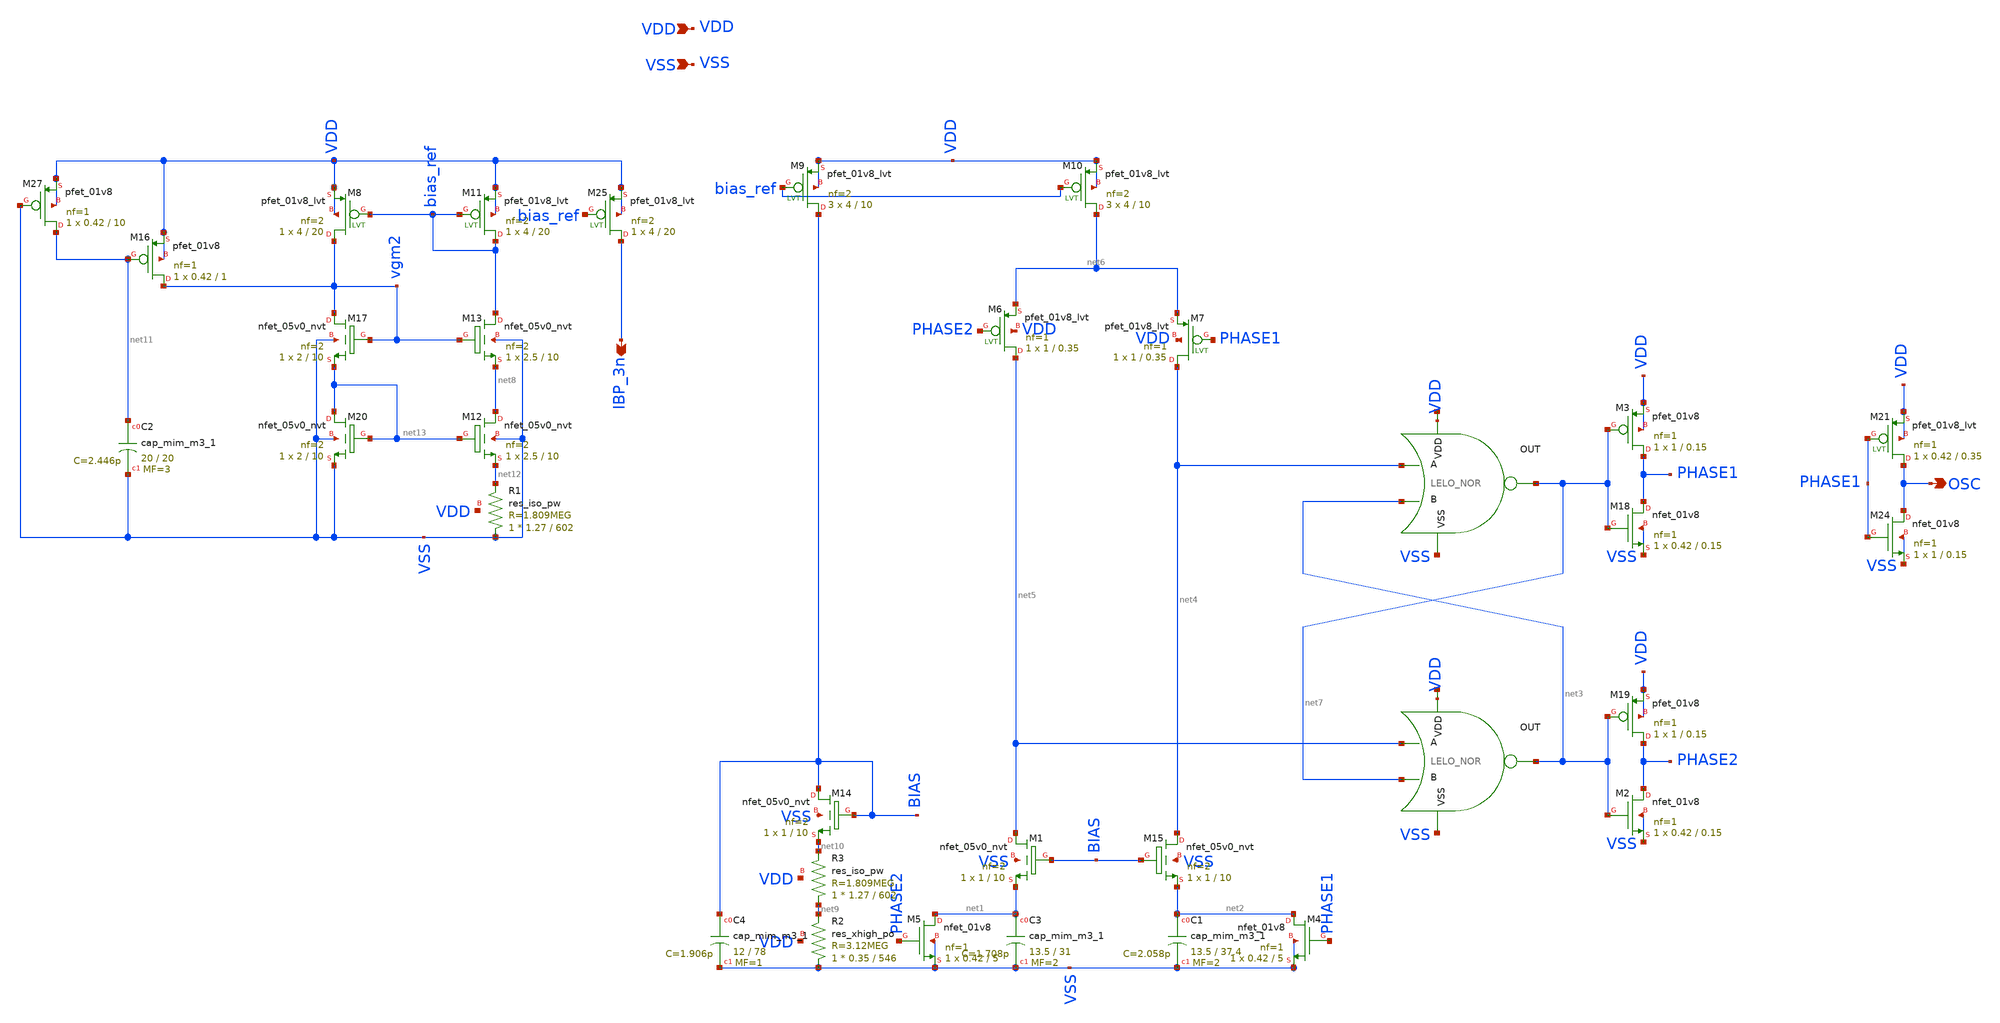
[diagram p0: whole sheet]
** sch_path: design/LELO_SVOD_SKY130A/LELO_SVOD_RELOSC.sch
**.subckt LELO_SVOD_RELOSC VDD VSS OSC IBP_3n
*.ipin VDD
*.ipin VSS
*.opin OSC
*.opin IBP_3n
x1 net14 net7 net4 net3 VSS LELO_NOR
x2 net15 net3 net5 net7 VSS LELO_NOR
XM6 net5 PHASE2 net6 VDD sky130_fd_pr__pfet_01v8_lvt L=0.35 W=1 nf=1 ad='int((1 + 1)/2) * 1 / 1 * 0.29'
+ as='int((1 + 2)/2) * 1 / 1 * 0.29' pd='2*int((1 + 1)/2) * (1 / 1 + 0.29)' ps='2*int((1 + 2)/2) * (1 / 1 + 0.29)'
+ nrd='0.29 / 1 ' nrs='0.29 / 1 ' sa=0 sb=0 sd=0 mult=1 m=1
XM7 net4 PHASE1 net6 VDD sky130_fd_pr__pfet_01v8_lvt L=0.35 W=1 nf=1 ad='int((1 + 1)/2) * 1 / 1 * 0.29'
+ as='int((1 + 2)/2) * 1 / 1 * 0.29' pd='2*int((1 + 1)/2) * (1 / 1 + 0.29)' ps='2*int((1 + 2)/2) * (1 / 1 + 0.29)'
+ nrd='0.29 / 1 ' nrs='0.29 / 1 ' sa=0 sb=0 sd=0 mult=1 m=1
XM11 bias_ref bias_ref VDD VDD sky130_fd_pr__pfet_01v8_lvt L=20 W=4 nf=2 ad='int((2 + 1)/2) * 4 / 2 * 0.29'
+ as='int((2 + 2)/2) * 4 / 2 * 0.29' pd='2*int((2 + 1)/2) * (4 / 2 + 0.29)' ps='2*int((2 + 2)/2) * (4 / 2 + 0.29)'
+ nrd='0.29 / 4 ' nrs='0.29 / 4 ' sa=0 sb=0 sd=0 mult=1 m=1
XC3 net1 VSS sky130_fd_pr__cap_mim_m3_1 W=13.5 L=31 MF=2 m=2
XC1 net2 VSS sky130_fd_pr__cap_mim_m3_1 W=13.5 L=37.4 MF=2 m=2
XM4 net2 PHASE1 VSS VSS sky130_fd_pr__nfet_01v8 L=5 W=0.42 nf=1 ad='int((1 + 1)/2) * 0.42 / 1 * 0.29'
+ as='int((1 + 2)/2) * 0.42 / 1 * 0.29' pd='2*int((1 + 1)/2) * (0.42 / 1 + 0.29)' ps='2*int((1 + 2)/2) * (0.42 / 1 + 0.29)'
+ nrd='0.29 / 0.42 ' nrs='0.29 / 0.42 ' sa=0 sb=0 sd=0 mult=1 m=1
XM5 net1 PHASE2 VSS VSS sky130_fd_pr__nfet_01v8 L=5 W=0.42 nf=1 ad='int((1 + 1)/2) * 0.42 / 1 * 0.29'
+ as='int((1 + 2)/2) * 0.42 / 1 * 0.29' pd='2*int((1 + 1)/2) * (0.42 / 1 + 0.29)' ps='2*int((1 + 2)/2) * (0.42 / 1 + 0.29)'
+ nrd='0.29 / 0.42 ' nrs='0.29 / 0.42 ' sa=0 sb=0 sd=0 mult=1 m=1
XM8 vgm2 bias_ref VDD VDD sky130_fd_pr__pfet_01v8_lvt L=20 W=4 nf=2 ad='int((2 + 1)/2) * 4 / 2 * 0.29'
+ as='int((2 + 2)/2) * 4 / 2 * 0.29' pd='2*int((2 + 1)/2) * (4 / 2 + 0.29)' ps='2*int((2 + 2)/2) * (4 / 2 + 0.29)'
+ nrd='0.29 / 4 ' nrs='0.29 / 4 ' sa=0 sb=0 sd=0 mult=1 m=1
XM9 BIAS bias_ref VDD VDD sky130_fd_pr__pfet_01v8_lvt L=10 W=4 nf=2 ad='int((2 + 1)/2) * 4 / 2 * 0.29'
+ as='int((2 + 2)/2) * 4 / 2 * 0.29' pd='2*int((2 + 1)/2) * (4 / 2 + 0.29)' ps='2*int((2 + 2)/2) * (4 / 2 + 0.29)'
+ nrd='0.29 / 4 ' nrs='0.29 / 4 ' sa=0 sb=0 sd=0 mult=3 m=3
XM10 net6 bias_ref VDD VDD sky130_fd_pr__pfet_01v8_lvt L=10 W=4 nf=2 ad='int((2 + 1)/2) * 4 / 2 * 0.29'
+ as='int((2 + 2)/2) * 4 / 2 * 0.29' pd='2*int((2 + 1)/2) * (4 / 2 + 0.29)' ps='2*int((2 + 2)/2) * (4 / 2 + 0.29)'
+ nrd='0.29 / 4 ' nrs='0.29 / 4 ' sa=0 sb=0 sd=0 mult=3 m=3
XM2 PHASE2 net3 VSS VSS sky130_fd_pr__nfet_01v8 L=0.15 W=0.42 nf=1 ad='int((1 + 1)/2) * 0.42 / 1 * 0.29'
+ as='int((1 + 2)/2) * 0.42 / 1 * 0.29' pd='2*int((1 + 1)/2) * (0.42 / 1 + 0.29)' ps='2*int((1 + 2)/2) * (0.42 / 1 + 0.29)'
+ nrd='0.29 / 0.42 ' nrs='0.29 / 0.42 ' sa=0 sb=0 sd=0 mult=1 m=1
XM18 PHASE1 net7 VSS VSS sky130_fd_pr__nfet_01v8 L=0.15 W=0.42 nf=1 ad='int((1 + 1)/2) * 0.42 / 1 * 0.29'
+ as='int((1 + 2)/2) * 0.42 / 1 * 0.29' pd='2*int((1 + 1)/2) * (0.42 / 1 + 0.29)' ps='2*int((1 + 2)/2) * (0.42 / 1 + 0.29)'
+ nrd='0.29 / 0.42 ' nrs='0.29 / 0.42 ' sa=0 sb=0 sd=0 mult=1 m=1
XM24 OSC PHASE1 VSS VSS sky130_fd_pr__nfet_01v8 L=0.15 W=1 nf=1 ad='int((1 + 1)/2) * 1 / 1 * 0.29' as='int((1 + 2)/2) * 1 / 1 * 0.29'
+ pd='2*int((1 + 1)/2) * (1 / 1 + 0.29)' ps='2*int((1 + 2)/2) * (1 / 1 + 0.29)' nrd='0.29 / 1 ' nrs='0.29 / 1 '
+ sa=0 sb=0 sd=0 mult=1 m=1
XM25 IBP_3n bias_ref VDD VDD sky130_fd_pr__pfet_01v8_lvt L=20 W=4 nf=2 ad='int((2 + 1)/2) * 4 / 2 * 0.29'
+ as='int((2 + 2)/2) * 4 / 2 * 0.29' pd='2*int((2 + 1)/2) * (4 / 2 + 0.29)' ps='2*int((2 + 2)/2) * (4 / 2 + 0.29)'
+ nrd='0.29 / 4 ' nrs='0.29 / 4 ' sa=0 sb=0 sd=0 mult=1 m=1
XM16 vgm2 net11 VDD VDD sky130_fd_pr__pfet_01v8 L=1 W=0.42 nf=1 ad='int((1 + 1)/2) * 0.42 / 1 * 0.29'
+ as='int((1 + 2)/2) * 0.42 / 1 * 0.29' pd='2*int((1 + 1)/2) * (0.42 / 1 + 0.29)' ps='2*int((1 + 2)/2) * (0.42 / 1 + 0.29)'
+ nrd='0.29 / 0.42 ' nrs='0.29 / 0.42 ' sa=0 sb=0 sd=0 mult=1 m=1
XM27 net11 VSS VDD VDD sky130_fd_pr__pfet_01v8 L=10 W=0.42 nf=1 ad='int((1 + 1)/2) * 0.42 / 1 * 0.29'
+ as='int((1 + 2)/2) * 0.42 / 1 * 0.29' pd='2*int((1 + 1)/2) * (0.42 / 1 + 0.29)' ps='2*int((1 + 2)/2) * (0.42 / 1 + 0.29)'
+ nrd='0.29 / 0.42 ' nrs='0.29 / 0.42 ' sa=0 sb=0 sd=0 mult=1 m=1
XC2 net11 VSS sky130_fd_pr__cap_mim_m3_1 W=20 L=20 MF=3 m=3
XM3 PHASE1 net7 VDD VDD sky130_fd_pr__pfet_01v8 L=0.15 W=1 nf=1 ad='int((1 + 1)/2) * 1 / 1 * 0.29' as='int((1 + 2)/2) * 1 / 1 * 0.29'
+ pd='2*int((1 + 1)/2) * (1 / 1 + 0.29)' ps='2*int((1 + 2)/2) * (1 / 1 + 0.29)' nrd='0.29 / 1 ' nrs='0.29 / 1 '
+ sa=0 sb=0 sd=0 mult=1 m=1
XM19 PHASE2 net3 VDD VDD sky130_fd_pr__pfet_01v8 L=0.15 W=1 nf=1 ad='int((1 + 1)/2) * 1 / 1 * 0.29' as='int((1 + 2)/2) * 1 / 1 * 0.29'
+ pd='2*int((1 + 1)/2) * (1 / 1 + 0.29)' ps='2*int((1 + 2)/2) * (1 / 1 + 0.29)' nrd='0.29 / 1 ' nrs='0.29 / 1 '
+ sa=0 sb=0 sd=0 mult=1 m=1
XC4 BIAS VSS sky130_fd_pr__cap_mim_m3_1 W=12 L=78 MF=1 m=1
XM1 net5 BIAS net1 VSS sky130_fd_pr__nfet_05v0_nvt L=10 W=1 nf=2 ad='int((2 + 1)/2) * 1 / 2 * 0.29' as='int((2 + 2)/2) * 1 / 2 * 0.29'
+ pd='2*int((2 + 1)/2) * (1 / 2 + 0.29)' ps='2*int((2 + 2)/2) * (1 / 2 + 0.29)' nrd='0.29 / 1 ' nrs='0.29 / 1 '
+ sa=0 sb=0 sd=0 mult=1 m=1
XM14 BIAS BIAS net10 VSS sky130_fd_pr__nfet_05v0_nvt L=10 W=1 nf=2 ad='int((2 + 1)/2) * 1 / 2 * 0.29'
+ as='int((2 + 2)/2) * 1 / 2 * 0.29' pd='2*int((2 + 1)/2) * (1 / 2 + 0.29)' ps='2*int((2 + 2)/2) * (1 / 2 + 0.29)'
+ nrd='0.29 / 1 ' nrs='0.29 / 1 ' sa=0 sb=0 sd=0 mult=1 m=1
XM15 net4 BIAS net2 VSS sky130_fd_pr__nfet_05v0_nvt L=10 W=1 nf=2 ad='int((2 + 1)/2) * 1 / 2 * 0.29'
+ as='int((2 + 2)/2) * 1 / 2 * 0.29' pd='2*int((2 + 1)/2) * (1 / 2 + 0.29)' ps='2*int((2 + 2)/2) * (1 / 2 + 0.29)'
+ nrd='0.29 / 1 ' nrs='0.29 / 1 ' sa=0 sb=0 sd=0 mult=1 m=1
XR3 net9 net10 VDD sky130_fd_pr__res_iso_pw W=1.27 L=602 m=1
XR2 VSS net9 VDD sky130_fd_pr__res_xhigh_po W=0.35 L=546 mult=1 m=1
XR1 VSS net12 VDD sky130_fd_pr__res_iso_pw W=1.27 L=602 m=1
XM13 bias_ref vgm2 net8 VSS sky130_fd_pr__nfet_05v0_nvt L=10 W=2.5 nf=2 ad='int((2 + 1)/2) * 2.5 / 2 * 0.29'
+ as='int((2 + 2)/2) * 2.5 / 2 * 0.29' pd='2*int((2 + 1)/2) * (2.5 / 2 + 0.29)' ps='2*int((2 + 2)/2) * (2.5 / 2 + 0.29)'
+ nrd='0.29 / 2.5 ' nrs='0.29 / 2.5 ' sa=0 sb=0 sd=0 mult=1 m=1
XM17 vgm2 vgm2 net13 VSS sky130_fd_pr__nfet_05v0_nvt L=10 W=2 nf=2 ad='int((2 + 1)/2) * 2 / 2 * 0.29'
+ as='int((2 + 2)/2) * 2 / 2 * 0.29' pd='2*int((2 + 1)/2) * (2 / 2 + 0.29)' ps='2*int((2 + 2)/2) * (2 / 2 + 0.29)'
+ nrd='0.29 / 2 ' nrs='0.29 / 2 ' sa=0 sb=0 sd=0 mult=1 m=1
XM20 net13 net13 VSS VSS sky130_fd_pr__nfet_05v0_nvt L=10 W=2 nf=2 ad='int((2 + 1)/2) * 2 / 2 * 0.29'
+ as='int((2 + 2)/2) * 2 / 2 * 0.29' pd='2*int((2 + 1)/2) * (2 / 2 + 0.29)' ps='2*int((2 + 2)/2) * (2 / 2 + 0.29)'
+ nrd='0.29 / 2 ' nrs='0.29 / 2 ' sa=0 sb=0 sd=0 mult=1 m=1
XM21 OSC PHASE1 VDD VDD sky130_fd_pr__pfet_01v8_lvt L=0.35 W=0.42 nf=1 ad='int((1 + 1)/2) * 0.42 / 1 * 0.29'
+ as='int((1 + 2)/2) * 0.42 / 1 * 0.29' pd='2*int((1 + 1)/2) * (0.42 / 1 + 0.29)' ps='2*int((1 + 2)/2) * (0.42 / 1 + 0.29)'
+ nrd='0.29 / 0.42 ' nrs='0.29 / 0.42 ' sa=0 sb=0 sd=0 mult=1 m=1
XM12 net8 net13 net12 VSS sky130_fd_pr__nfet_05v0_nvt L=10 W=2.5 nf=2 ad='int((2 + 1)/2) * 2.5 / 2 * 0.29'
+ as='int((2 + 2)/2) * 2.5 / 2 * 0.29' pd='2*int((2 + 1)/2) * (2.5 / 2 + 0.29)' ps='2*int((2 + 2)/2) * (2.5 / 2 + 0.29)'
+ nrd='0.29 / 2.5 ' nrs='0.29 / 2.5 ' sa=0 sb=0 sd=0 mult=1 m=1
**.ends

* expanding   symbol:  LELO_SVOD_SKY130A/LELO_NOR.sym # of pins=5
** sym_path: design/LELO_SVOD_SKY130A/LELO_NOR.sym
** sch_path: design/LELO_SVOD_SKY130A/LELO_NOR.sch
.subckt LELO_NOR VDD OUT A B VSS
*.ipin VDD
*.ipin VSS
*.opin OUT
*.ipin A
*.ipin B
XM2 OUT B VSS VSS sky130_fd_pr__nfet_01v8 L=0.15 W=2 nf=1 ad='int((1 + 1)/2) * 2 / 1 * 0.29' as='int((1 + 2)/2) * 2 / 1 * 0.29'
+ pd='2*int((1 + 1)/2) * (2 / 1 + 0.29)' ps='2*int((1 + 2)/2) * (2 / 1 + 0.29)' nrd='0.29 / 2 ' nrs='0.29 / 2 '
+ sa=0 sb=0 sd=0 mult=1 m=1
XM1 OUT A VSS VSS sky130_fd_pr__nfet_01v8 L=0.15 W=2 nf=1 ad='int((1 + 1)/2) * 2 / 1 * 0.29' as='int((1 + 2)/2) * 2 / 1 * 0.29'
+ pd='2*int((1 + 1)/2) * (2 / 1 + 0.29)' ps='2*int((1 + 2)/2) * (2 / 1 + 0.29)' nrd='0.29 / 2 ' nrs='0.29 / 2 '
+ sa=0 sb=0 sd=0 mult=1 m=1
XM3 OUT B net1 VDD sky130_fd_pr__pfet_01v8 L=0.15 W=4 nf=1 ad='int((1 + 1)/2) * 4 / 1 * 0.29' as='int((1 + 2)/2) * 4 / 1 * 0.29'
+ pd='2*int((1 + 1)/2) * (4 / 1 + 0.29)' ps='2*int((1 + 2)/2) * (4 / 1 + 0.29)' nrd='0.29 / 4 ' nrs='0.29 / 4 '
+ sa=0 sb=0 sd=0 mult=1 m=1
XM4 net1 A VDD VDD sky130_fd_pr__pfet_01v8 L=0.15 W=4 nf=1 ad='int((1 + 1)/2) * 4 / 1 * 0.29' as='int((1 + 2)/2) * 4 / 1 * 0.29'
+ pd='2*int((1 + 1)/2) * (4 / 1 + 0.29)' ps='2*int((1 + 2)/2) * (4 / 1 + 0.29)' nrd='0.29 / 4 ' nrs='0.29 / 4 '
+ sa=0 sb=0 sd=0 mult=1 m=1
.ends

.end
